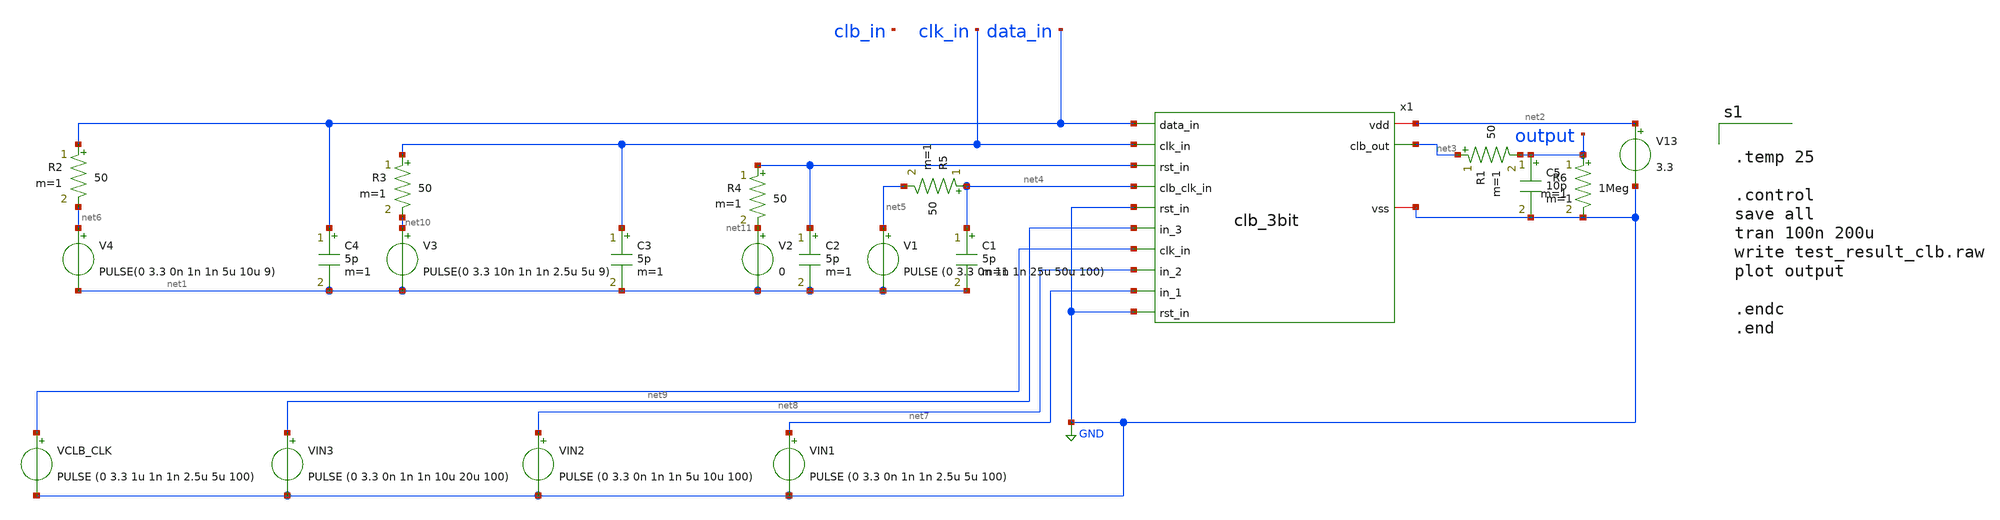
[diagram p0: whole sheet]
** sch_path: designs/libs/tb_fpga/tb_clb/clb_3bit_tb.sch
**.subckt clb_3bit_tb
C1 net4 net1 5p m=1
C2 GND net1 5p m=1
C3 clk_in net1 5p m=1
C4 data_in net1 5p m=1
V1 net5 net1 PULSE (0 3.3 0n 1n 1n 25u 50u 100)
V2 net11 net1 0
V3 net10 net1 PULSE(0 3.3 10n 1n 1n 2.5u 5u 9)
V4 net6 net1 PULSE(0 3.3 0n 1n 1n 5u 10u 9)
V13 net2 GND 3.3
C5 output GND 10p m=1
R1 net3 output 50 m=1
R2 data_in net6 50 m=1
R3 clk_in net10 50 m=1
R4 GND net11 50 m=1
R5 net4 net5 50 m=1
R6 output GND 1Meg m=1
VIN1 net7 GND PULSE (0 3.3 0n 1n 1n 2.5u 5u 100)
VIN2 net8 GND PULSE (0 3.3 0n 1n 1n 5u 10u 100)
VIN3 net9 GND PULSE (0 3.3 0n 1n 1n 10u 20u 100)
VCLB_CLK clk_in GND PULSE (0 3.3 1u 1n 1n 2.5u 5u 100)
x1 data_in clk_in net2 GND net3 net4 net9 net8 net7 GND clb_3bit
**** begin user architecture code


.temp 25

.control
save all
tran 100n 200u
write test_result_clb.raw
plot output

.endc
.end



.include $::180MCU_MODELS/design.ngspice
.lib $::180MCU_MODELS/sm141064.ngspice typical
.lib $::180MCU_MODELS/sm141064.ngspice cap_mim
.lib $::180MCU_MODELS/sm141064.ngspice res_typical
.lib $::180MCU_MODELS/sm141064.ngspice moscap_typical
.lib $::180MCU_MODELS/sm141064.ngspice mimcap_typical
* .lib $::180MCU_MODELS/sm141064.ngspice res_statistical

**** end user architecture code
**.ends
.GLOBAL GND
.end
